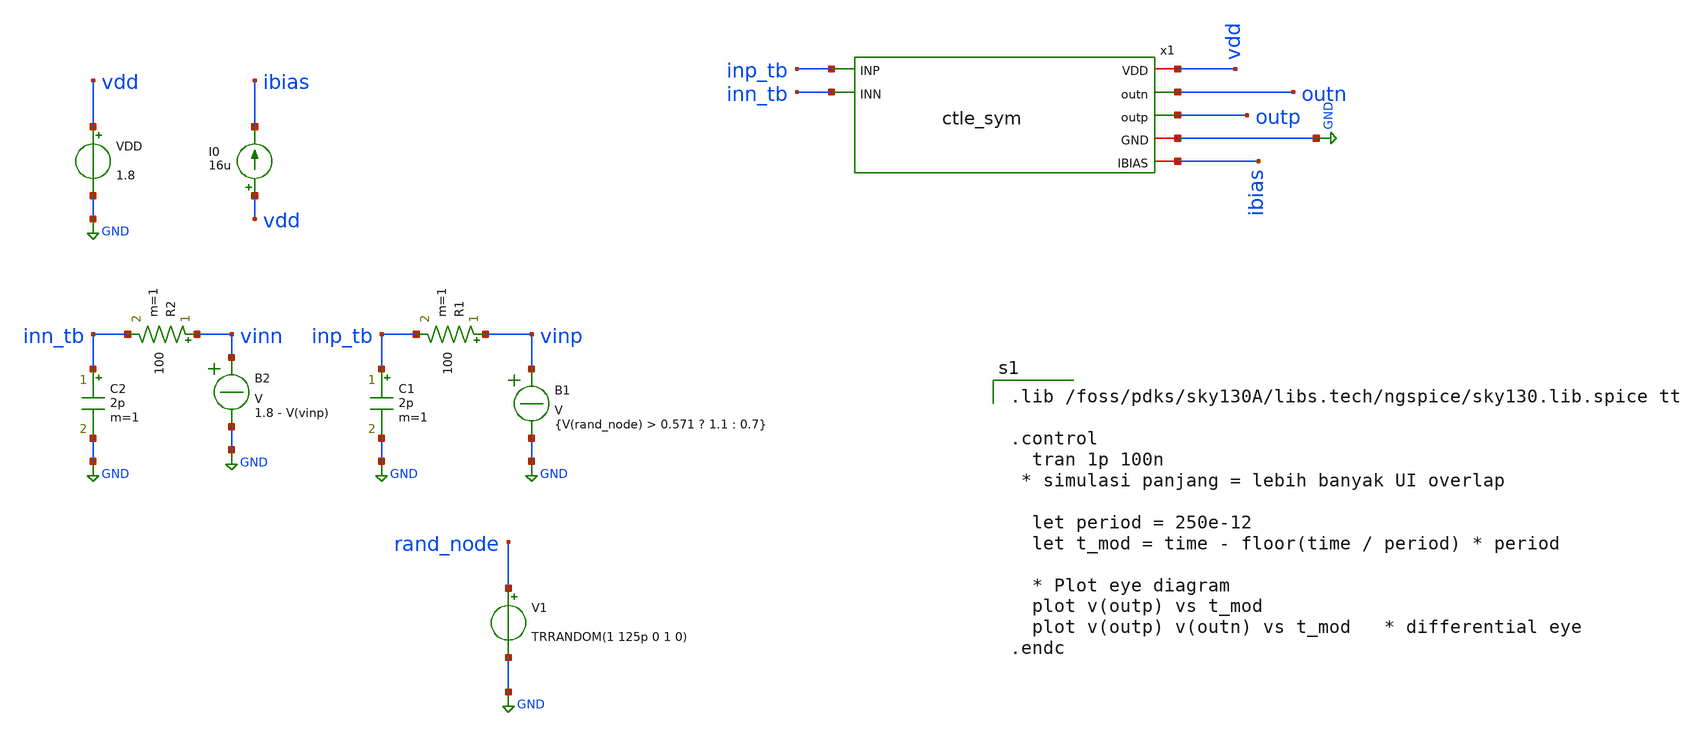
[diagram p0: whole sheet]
** sch_path: CTLE/tb_eye.sch
**.subckt tb_eye
R1 vinp inp_tb 100 m=1
C1 inp_tb GND 2p m=1
V1 rand_node GND TRRANDOM(1 125p 0 1 0)
R2 vinn inn_tb 100 m=1
C2 inn_tb GND 2p m=1
VDD vdd GND 1.8
I0 vdd ibias 16u
x1 vdd outn outp inp_tb inn_tb GND ibias ctle_sym
B1 vinp GND V = {V(rand_node) > 0.571 ? 1.1 : 0.7}
B2 vinn GND V = 1.8 - V(vinp)
**** begin user architecture code

.lib /foss/pdks/sky130A/libs.tech/ngspice/sky130.lib.spice tt

.control
  tran 1p 100n
 * simulasi panjang = lebih banyak UI overlap

  let period = 250e-12
  let t_mod = time - floor(time / period) * period

  * Plot eye diagram
  plot v(outp) vs t_mod
  plot v(outp) v(outn) vs t_mod   * differential eye
.endc


**** end user architecture code
**.ends

* expanding   symbol:  ctle_sym.sym # of pins=7
** sym_path: CTLE/ctle_sym.sym
** sch_path: CTLE/ctle_sym.sch
.subckt ctle_sym VDD outn outp INP INN GND IBIAS
*.opin outp
*.opin outn
*.ipin INN
*.iopin VDD
*.iopin GND
*.iopin IBIAS
*.ipin INP
XM1 outp INP net1 GND sky130_fd_pr__nfet_01v8_lvt L=0.15 W=2 nf=1 ad='int((nf+1)/2) * W/nf * 0.29' as='int((nf+2)/2) * W/nf * 0.29'
+ pd='2*int((nf+1)/2) * (W/nf + 0.29)' ps='2*int((nf+2)/2) * (W/nf + 0.29)' nrd='0.29 / W' nrs='0.29 / W'
+ sa=0 sb=0 sd=0 mult=15 m=15
XM2 outn INN net2 GND sky130_fd_pr__nfet_01v8_lvt L=0.15 W=2 nf=1 ad='int((nf+1)/2) * W/nf * 0.29' as='int((nf+2)/2) * W/nf * 0.29'
+ pd='2*int((nf+1)/2) * (W/nf + 0.29)' ps='2*int((nf+2)/2) * (W/nf + 0.29)' nrd='0.29 / W' nrs='0.29 / W'
+ sa=0 sb=0 sd=0 mult=15 m=15
XM3 net1 IBIAS GND GND sky130_fd_pr__nfet_01v8_lvt L=1 W=2 nf=1 ad='int((nf+1)/2) * W/nf * 0.29' as='int((nf+2)/2) * W/nf * 0.29'
+ pd='2*int((nf+1)/2) * (W/nf + 0.29)' ps='2*int((nf+2)/2) * (W/nf + 0.29)' nrd='0.29 / W' nrs='0.29 / W'
+ sa=0 sb=0 sd=0 mult=24 m=24
XM4 net2 IBIAS GND GND sky130_fd_pr__nfet_01v8_lvt L=1 W=2 nf=1 ad='int((nf+1)/2) * W/nf * 0.29' as='int((nf+2)/2) * W/nf * 0.29'
+ pd='2*int((nf+1)/2) * (W/nf + 0.29)' ps='2*int((nf+2)/2) * (W/nf + 0.29)' nrd='0.29 / W' nrs='0.29 / W'
+ sa=0 sb=0 sd=0 mult=24 m=24
XM5 IBIAS IBIAS GND GND sky130_fd_pr__nfet_01v8_lvt L=1 W=2 nf=1 ad='int((nf+1)/2) * W/nf * 0.29' as='int((nf+2)/2) * W/nf * 0.29'
+ pd='2*int((nf+1)/2) * (W/nf + 0.29)' ps='2*int((nf+2)/2) * (W/nf + 0.29)' nrd='0.29 / W' nrs='0.29 / W'
+ sa=0 sb=0 sd=0 mult=1 m=1
RD1 VDD outp 280 m=1
RD2 VDD outn 280 m=1
CS net1 net2 134f m=1
RS net1 net2 1400 m=1
C1 outp GND 20f m=1
C2 outn GND 20f m=1
.ends

.GLOBAL GND
.end
